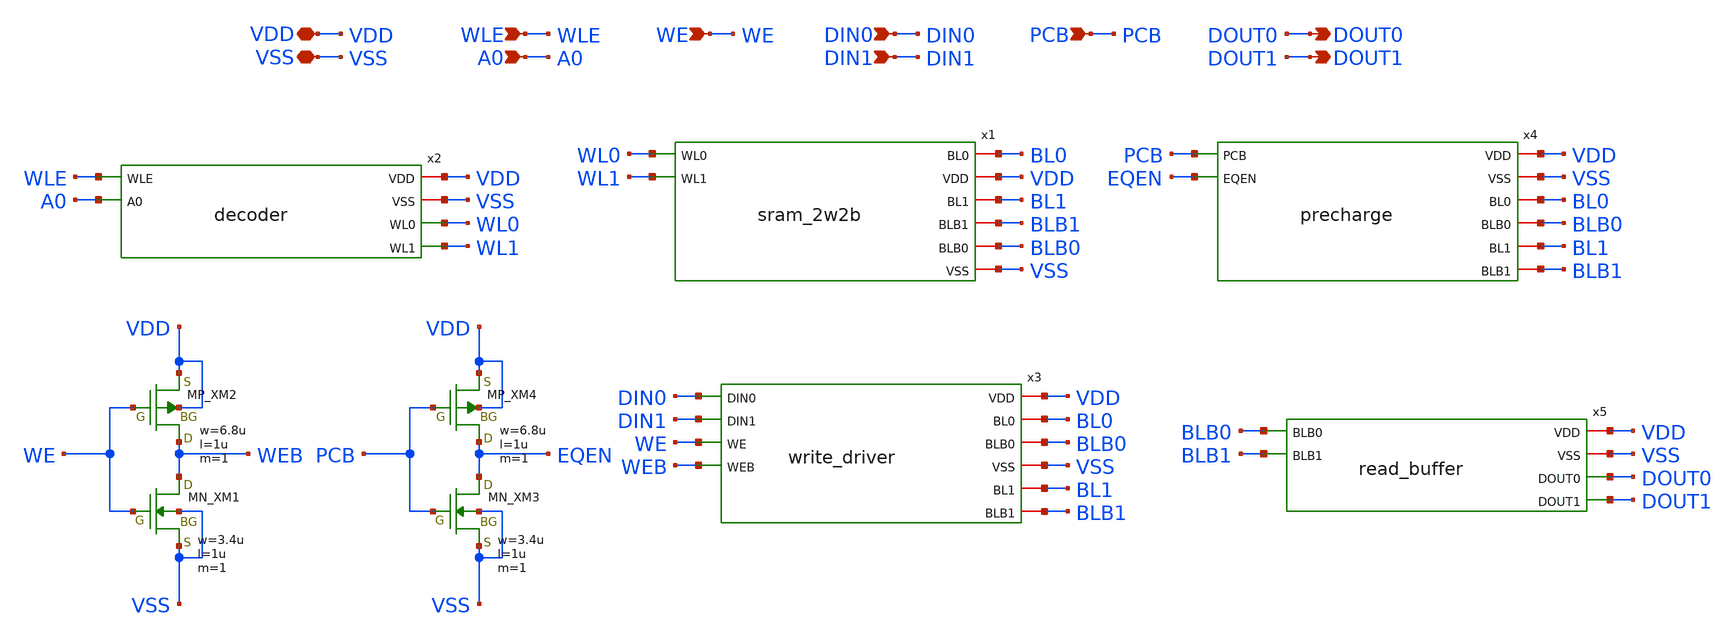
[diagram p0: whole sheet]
** sch_path: Deliverables/sram_2w2b_top.sch
**.subckt sram_2w2b_top VDD WLE DOUT0 VSS A0 WE DIN0 DIN1 PCB DOUT1
*.iopin VDD
*.ipin WLE
*.opin DOUT0
*.iopin VSS
*.ipin A0
*.ipin WE
*.ipin DIN0
*.ipin DIN1
*.ipin PCB
*.opin DOUT1
x1 WL0 BL0 VDD BL1 BLB1 WL1 BLB0 VSS sram_2w2b
x2 VDD VSS WL0 WLE A0 WL1 decoder
x3 DIN0 VDD BL0 BLB0 VSS DIN1 BL1 WE BLB1 WEB write_driver
x4 VDD VSS PCB EQEN BL0 BLB0 BL1 BLB1 precharge
x5 VDD VSS BLB0 BLB1 DOUT0 DOUT1 read_buffer
XXM1 WEB WE VSS VSS NMOS w=3.4u l=1u nrd=0 nrs=0 m=1
XXM2 WEB WE VDD VDD PMOS w=6.8u l=1u nrd=0 nrs=0 m=1
XXM3 EQEN PCB VSS VSS NMOS w=3.4u l=1u nrd=0 nrs=0 m=1
XXM4 EQEN PCB VDD VDD PMOS w=6.8u l=1u nrd=0 nrs=0 m=1
**.ends
.end
